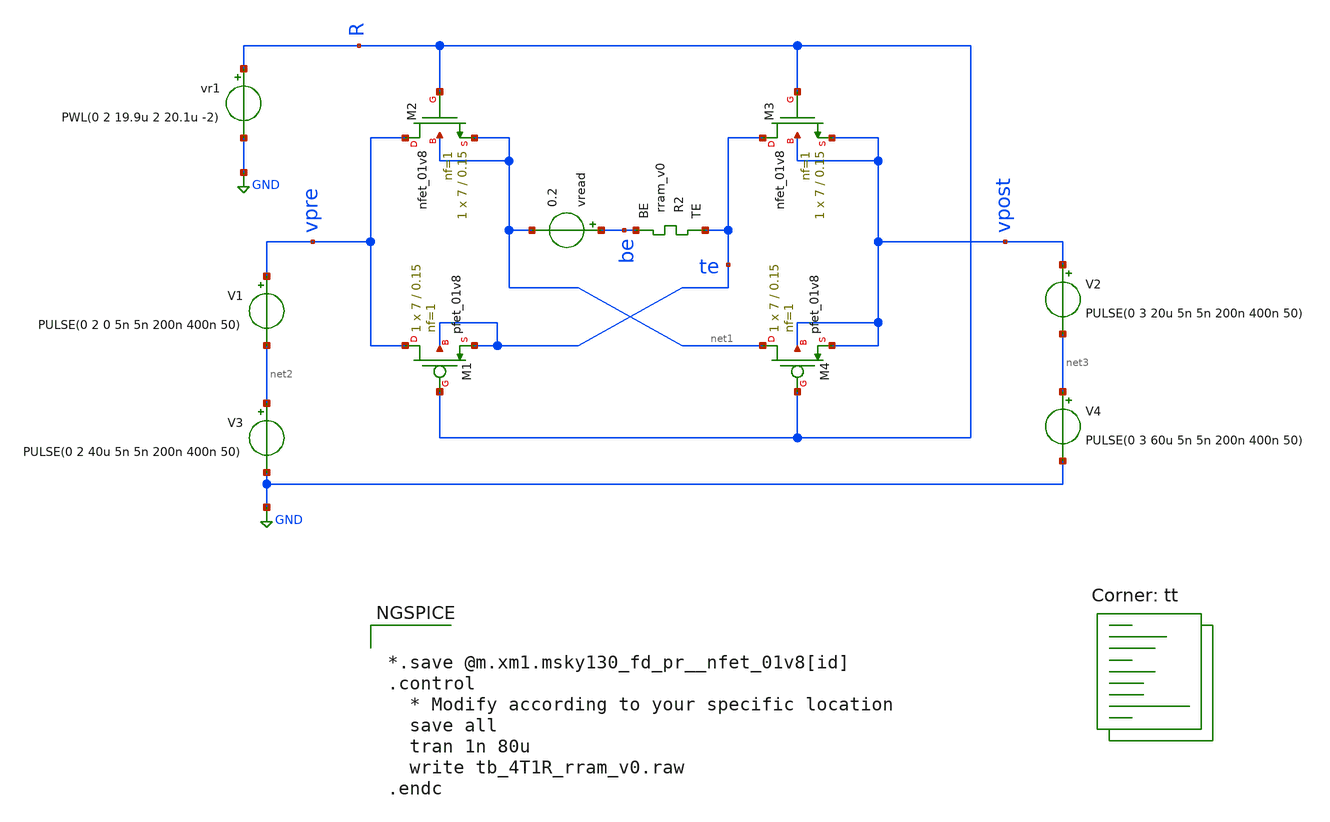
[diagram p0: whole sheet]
** sch_path: Synapse/tb_4T1R_rram_v0.sch
**.subckt tb_4T1R_rram_v0
XR2 te be rram_v0
XM2 vpre R net1 net1 sky130_fd_pr__nfet_01v8 L=0.15 W=7 nf=1 ad='int((nf+1)/2) * W/nf * 0.29' as='int((nf+2)/2) * W/nf * 0.29'
+ pd='2*int((nf+1)/2) * (W/nf + 0.29)' ps='2*int((nf+2)/2) * (W/nf + 0.29)' nrd='0.29 / W' nrs='0.29 / W'
+ sa=0 sb=0 sd=0 mult=1 m=1
XM3 te R vpost vpost sky130_fd_pr__nfet_01v8 L=0.15 W=7 nf=1 ad='int((nf+1)/2) * W/nf * 0.29' as='int((nf+2)/2) * W/nf * 0.29'
+ pd='2*int((nf+1)/2) * (W/nf + 0.29)' ps='2*int((nf+2)/2) * (W/nf + 0.29)' nrd='0.29 / W' nrs='0.29 / W'
+ sa=0 sb=0 sd=0 mult=1 m=1
V1 vpre net2 PULSE(0 2 0 5n 5n 200n 400n 50)
V2 vpost net3 PULSE(0 3 20u 5n 5n 200n 400n 50)
V3 net2 GND PULSE(0 2 40u 5n 5n 200n 400n 50)
V4 net3 GND PULSE(0 3 60u 5n 5n 200n 400n 50)
vread be net1 0.2
vr1 R GND PWL(0 2 19.9u 2 20.1u -2)
XM1 vpre R te te sky130_fd_pr__pfet_01v8 L=0.15 W=7 nf=1 ad='int((nf+1)/2) * W/nf * 0.29' as='int((nf+2)/2) * W/nf * 0.29'
+ pd='2*int((nf+1)/2) * (W/nf + 0.29)' ps='2*int((nf+2)/2) * (W/nf + 0.29)' nrd='0.29 / W' nrs='0.29 / W'
+ sa=0 sb=0 sd=0 mult=1 m=1
XM4 net1 R vpost vpost sky130_fd_pr__pfet_01v8 L=0.15 W=7 nf=1 ad='int((nf+1)/2) * W/nf * 0.29' as='int((nf+2)/2) * W/nf * 0.29'
+ pd='2*int((nf+1)/2) * (W/nf + 0.29)' ps='2*int((nf+2)/2) * (W/nf + 0.29)' nrd='0.29 / W' nrs='0.29 / W'
+ sa=0 sb=0 sd=0 mult=1 m=1
**** begin user architecture code


*.save @m.xm1.msky130_fd_pr__nfet_01v8[id]
.control
  * Modify according to your specific location
  save all
  tran 1n 80u
  write tb_4T1R_rram_v0.raw
.endc



.lib $::SKYWATER_MODELS/sky130.lib.spice tt

** opencircuitdesign pdks install
.inc $::SKYWATER_MODELS/rram_v0.spice

**** end user architecture code
**.ends
.GLOBAL GND
.end
